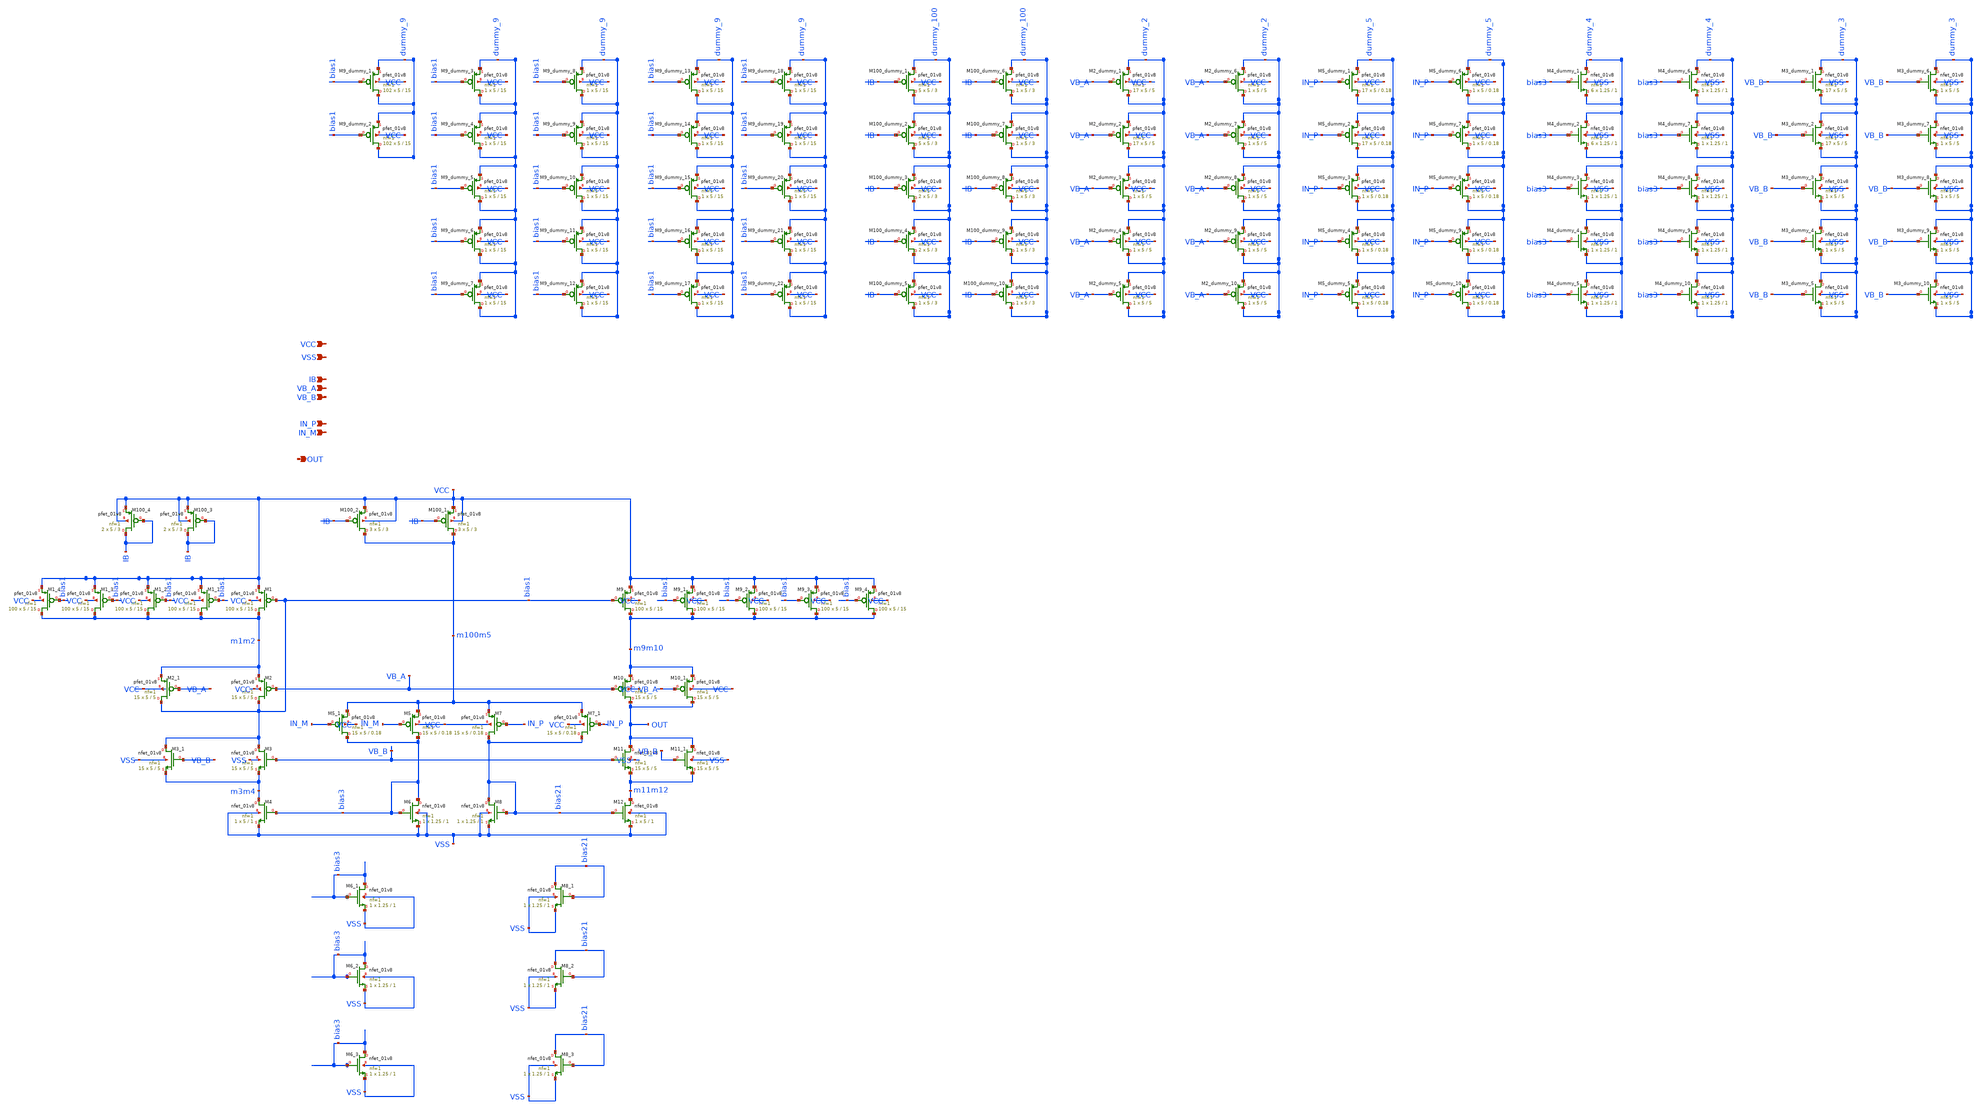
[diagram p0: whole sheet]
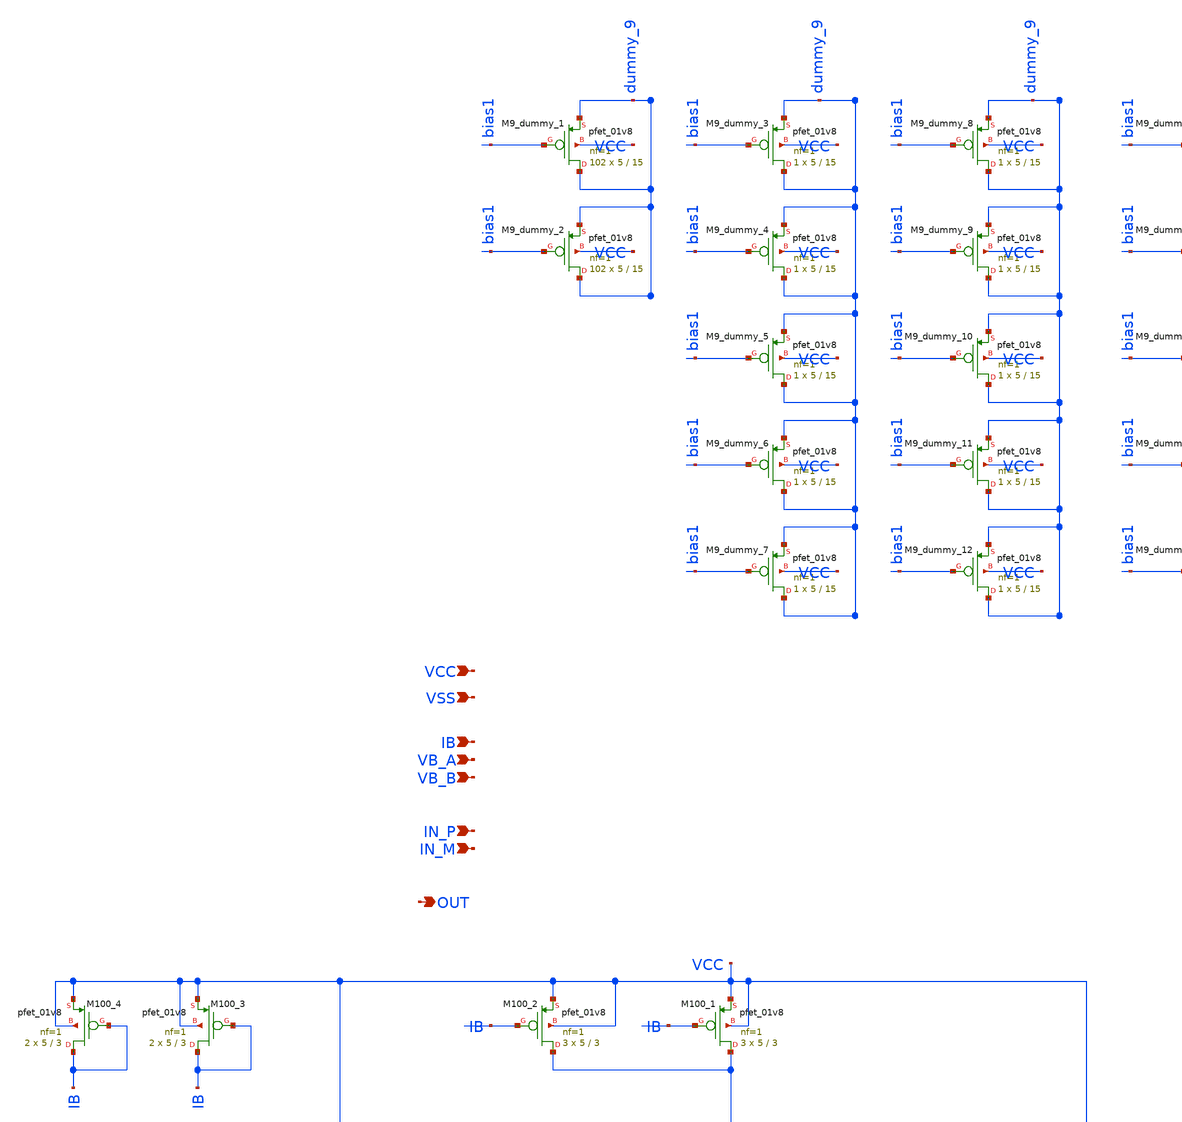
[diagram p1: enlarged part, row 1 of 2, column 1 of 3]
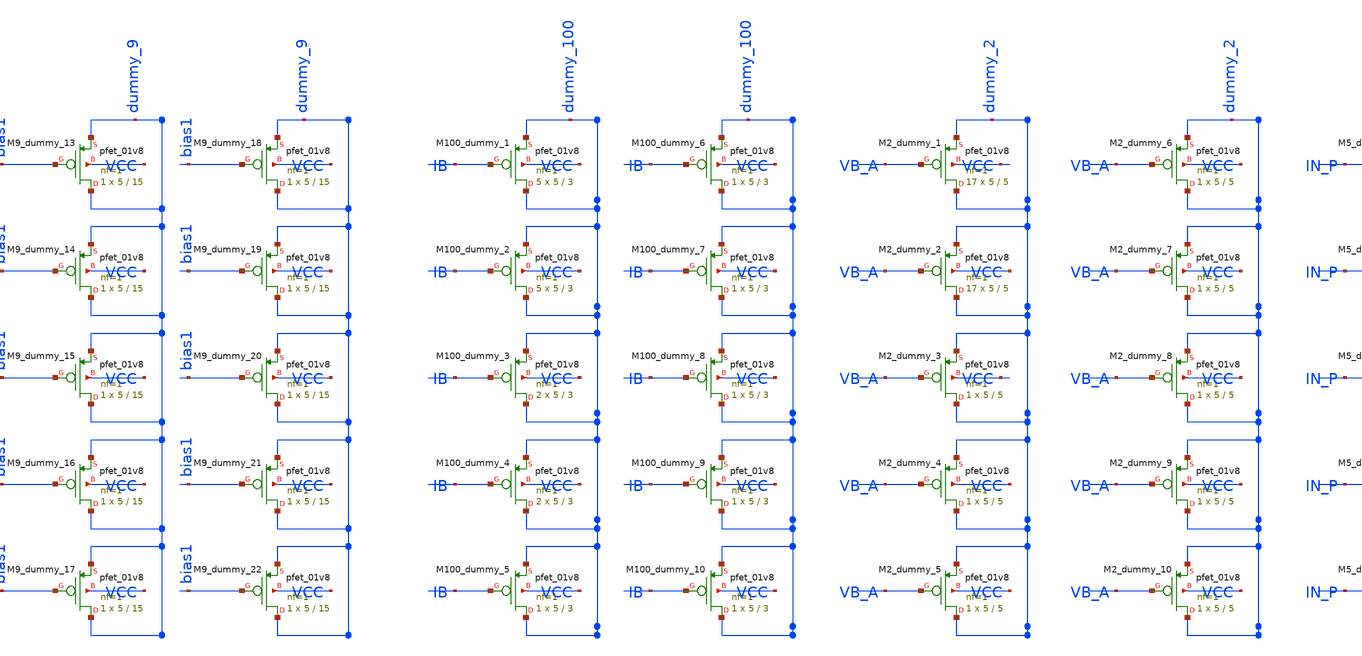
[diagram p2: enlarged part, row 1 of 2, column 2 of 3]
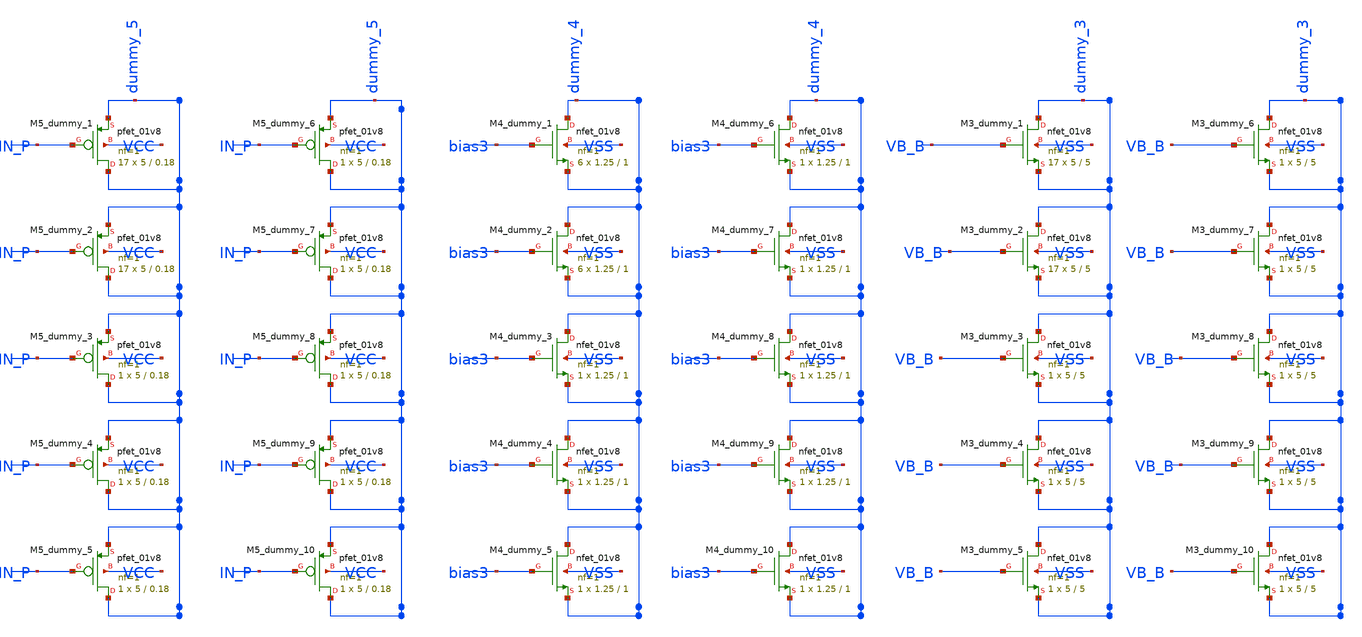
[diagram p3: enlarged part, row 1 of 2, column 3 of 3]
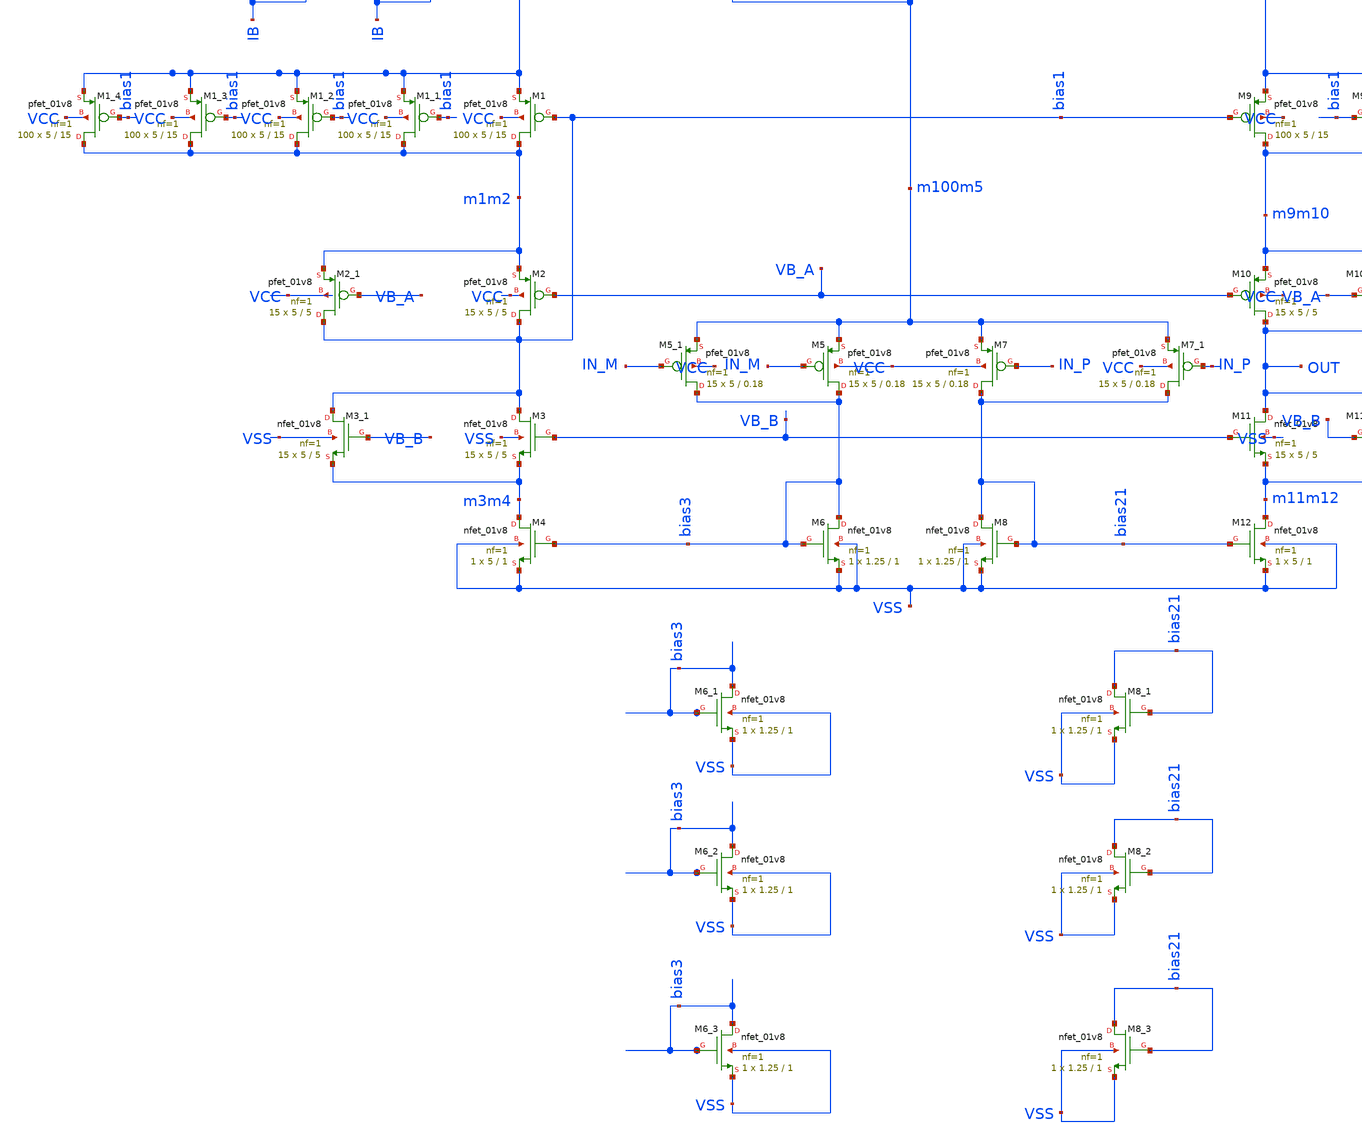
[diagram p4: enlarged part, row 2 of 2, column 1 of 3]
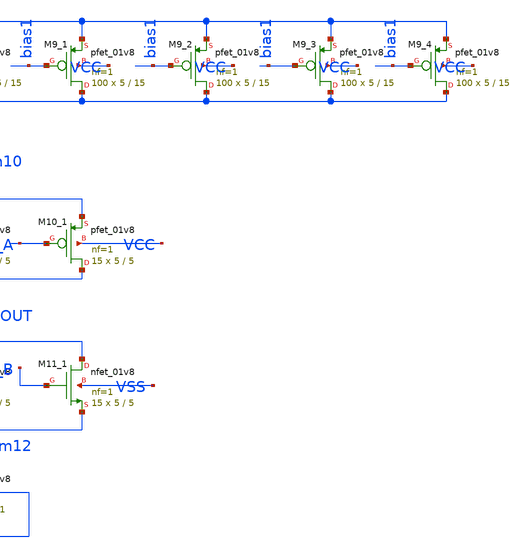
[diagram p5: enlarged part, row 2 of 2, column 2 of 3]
** sch_path: 03_Layout/opamp_cascode.sch
**.subckt opamp_cascode IN_P IN_M VCC VSS OUT VB_A VB_B IB
*.ipin IN_P
*.ipin IN_M
*.ipin VCC
*.ipin VSS
*.opin OUT
*.ipin VB_A
*.ipin VB_B
*.ipin IB
XM100_3 IB IB VCC VCC sky130_fd_pr__pfet_01v8 L=3 W=5 nf=1 ad='int((nf+1)/2) * W/nf * 0.29' as='int((nf+2)/2) * W/nf * 0.29'
+ pd='2*int((nf+1)/2) * (W/nf + 0.29)' ps='2*int((nf+2)/2) * (W/nf + 0.29)' nrd='0.29 / W' nrs='0.29 / W'
+ sa=0 sb=0 sd=0 mult=2 m=2
XM10 OUT VB_A m9m10 VCC sky130_fd_pr__pfet_01v8 L=5 W=5 nf=1 ad='int((nf+1)/2) * W/nf * 0.29' as='int((nf+2)/2) * W/nf * 0.29'
+ pd='2*int((nf+1)/2) * (W/nf + 0.29)' ps='2*int((nf+2)/2) * (W/nf + 0.29)' nrd='0.29 / W' nrs='0.29 / W'
+ sa=0 sb=0 sd=0 mult=15 m=15
XM2 bias1 VB_A m1m2 VCC sky130_fd_pr__pfet_01v8 L=5 W=5 nf=1 ad='int((nf+1)/2) * W/nf * 0.29' as='int((nf+2)/2) * W/nf * 0.29'
+ pd='2*int((nf+1)/2) * (W/nf + 0.29)' ps='2*int((nf+2)/2) * (W/nf + 0.29)' nrd='0.29 / W' nrs='0.29 / W'
+ sa=0 sb=0 sd=0 mult=15 m=15
XM5 bias3 IN_M m100m5 VCC sky130_fd_pr__pfet_01v8 L=0.18 W=5 nf=1 ad='int((nf+1)/2) * W/nf * 0.29' as='int((nf+2)/2) * W/nf * 0.29'
+ pd='2*int((nf+1)/2) * (W/nf + 0.29)' ps='2*int((nf+2)/2) * (W/nf + 0.29)' nrd='0.29 / W' nrs='0.29 / W'
+ sa=0 sb=0 sd=0 mult=15 m=15
XM7 bias21 IN_P m100m5 VCC sky130_fd_pr__pfet_01v8 L=0.18 W=5 nf=1 ad='int((nf+1)/2) * W/nf * 0.29' as='int((nf+2)/2) * W/nf * 0.29'
+ pd='2*int((nf+1)/2) * (W/nf + 0.29)' ps='2*int((nf+2)/2) * (W/nf + 0.29)' nrd='0.29 / W' nrs='0.29 / W'
+ sa=0 sb=0 sd=0 mult=15 m=15
XM6 bias3 bias3 VSS VSS sky130_fd_pr__nfet_01v8 L=1 W=1.25 nf=1 ad='int((nf+1)/2) * W/nf * 0.29' as='int((nf+2)/2) * W/nf * 0.29'
+ pd='2*int((nf+1)/2) * (W/nf + 0.29)' ps='2*int((nf+2)/2) * (W/nf + 0.29)' nrd='0.29 / W' nrs='0.29 / W'
+ sa=0 sb=0 sd=0 mult=1 m=1
XM8 bias21 bias21 VSS VSS sky130_fd_pr__nfet_01v8 L=1 W=1.25 nf=1 ad='int((nf+1)/2) * W/nf * 0.29' as='int((nf+2)/2) * W/nf * 0.29'
+ pd='2*int((nf+1)/2) * (W/nf + 0.29)' ps='2*int((nf+2)/2) * (W/nf + 0.29)' nrd='0.29 / W' nrs='0.29 / W'
+ sa=0 sb=0 sd=0 mult=1 m=1
XM12 m11m12 bias21 VSS VSS sky130_fd_pr__nfet_01v8 L=1 W=5 nf=1 ad='int((nf+1)/2) * W/nf * 0.29' as='int((nf+2)/2) * W/nf * 0.29'
+ pd='2*int((nf+1)/2) * (W/nf + 0.29)' ps='2*int((nf+2)/2) * (W/nf + 0.29)' nrd='0.29 / W' nrs='0.29 / W'
+ sa=0 sb=0 sd=0 mult=1 m=1
XM11 OUT VB_B m11m12 VSS sky130_fd_pr__nfet_01v8 L=5 W=5 nf=1 ad='int((nf+1)/2) * W/nf * 0.29' as='int((nf+2)/2) * W/nf * 0.29'
+ pd='2*int((nf+1)/2) * (W/nf + 0.29)' ps='2*int((nf+2)/2) * (W/nf + 0.29)' nrd='0.29 / W' nrs='0.29 / W'
+ sa=0 sb=0 sd=0 mult=15 m=15
XM3 bias1 VB_B m3m4 VSS sky130_fd_pr__nfet_01v8 L=5 W=5 nf=1 ad='int((nf+1)/2) * W/nf * 0.29' as='int((nf+2)/2) * W/nf * 0.29'
+ pd='2*int((nf+1)/2) * (W/nf + 0.29)' ps='2*int((nf+2)/2) * (W/nf + 0.29)' nrd='0.29 / W' nrs='0.29 / W'
+ sa=0 sb=0 sd=0 mult=15 m=15
XM100_1 m100m5 IB VCC VCC sky130_fd_pr__pfet_01v8 L=3 W=5 nf=1 ad='int((nf+1)/2) * W/nf * 0.29' as='int((nf+2)/2) * W/nf * 0.29'
+ pd='2*int((nf+1)/2) * (W/nf + 0.29)' ps='2*int((nf+2)/2) * (W/nf + 0.29)' nrd='0.29 / W' nrs='0.29 / W'
+ sa=0 sb=0 sd=0 mult=3 m=3
XM5_1 bias3 IN_M m100m5 VCC sky130_fd_pr__pfet_01v8 L=0.18 W=5 nf=1 ad='int((nf+1)/2) * W/nf * 0.29'
+ as='int((nf+2)/2) * W/nf * 0.29' pd='2*int((nf+1)/2) * (W/nf + 0.29)' ps='2*int((nf+2)/2) * (W/nf + 0.29)'
+ nrd='0.29 / W' nrs='0.29 / W' sa=0 sb=0 sd=0 mult=15 m=15
XM7_1 bias21 IN_P m100m5 VCC sky130_fd_pr__pfet_01v8 L=0.18 W=5 nf=1 ad='int((nf+1)/2) * W/nf * 0.29'
+ as='int((nf+2)/2) * W/nf * 0.29' pd='2*int((nf+1)/2) * (W/nf + 0.29)' ps='2*int((nf+2)/2) * (W/nf + 0.29)'
+ nrd='0.29 / W' nrs='0.29 / W' sa=0 sb=0 sd=0 mult=15 m=15
XM9 m9m10 bias1 VCC VCC sky130_fd_pr__pfet_01v8 L=15 W=5 nf=1 ad='int((nf+1)/2) * W/nf * 0.29' as='int((nf+2)/2) * W/nf * 0.29'
+ pd='2*int((nf+1)/2) * (W/nf + 0.29)' ps='2*int((nf+2)/2) * (W/nf + 0.29)' nrd='0.29 / W' nrs='0.29 / W'
+ sa=0 sb=0 sd=0 mult=100 m=100
XM9_1 m9m10 bias1 VCC VCC sky130_fd_pr__pfet_01v8 L=15 W=5 nf=1 ad='int((nf+1)/2) * W/nf * 0.29' as='int((nf+2)/2) * W/nf * 0.29'
+ pd='2*int((nf+1)/2) * (W/nf + 0.29)' ps='2*int((nf+2)/2) * (W/nf + 0.29)' nrd='0.29 / W' nrs='0.29 / W'
+ sa=0 sb=0 sd=0 mult=100 m=100
XM9_2 m9m10 bias1 VCC VCC sky130_fd_pr__pfet_01v8 L=15 W=5 nf=1 ad='int((nf+1)/2) * W/nf * 0.29' as='int((nf+2)/2) * W/nf * 0.29'
+ pd='2*int((nf+1)/2) * (W/nf + 0.29)' ps='2*int((nf+2)/2) * (W/nf + 0.29)' nrd='0.29 / W' nrs='0.29 / W'
+ sa=0 sb=0 sd=0 mult=100 m=100
XM9_3 m9m10 bias1 VCC VCC sky130_fd_pr__pfet_01v8 L=15 W=5 nf=1 ad='int((nf+1)/2) * W/nf * 0.29' as='int((nf+2)/2) * W/nf * 0.29'
+ pd='2*int((nf+1)/2) * (W/nf + 0.29)' ps='2*int((nf+2)/2) * (W/nf + 0.29)' nrd='0.29 / W' nrs='0.29 / W'
+ sa=0 sb=0 sd=0 mult=100 m=100
XM9_4 m9m10 bias1 VCC VCC sky130_fd_pr__pfet_01v8 L=15 W=5 nf=1 ad='int((nf+1)/2) * W/nf * 0.29' as='int((nf+2)/2) * W/nf * 0.29'
+ pd='2*int((nf+1)/2) * (W/nf + 0.29)' ps='2*int((nf+2)/2) * (W/nf + 0.29)' nrd='0.29 / W' nrs='0.29 / W'
+ sa=0 sb=0 sd=0 mult=100 m=100
XM1 m1m2 bias1 VCC VCC sky130_fd_pr__pfet_01v8 L=15 W=5 nf=1 ad='int((nf+1)/2) * W/nf * 0.29' as='int((nf+2)/2) * W/nf * 0.29'
+ pd='2*int((nf+1)/2) * (W/nf + 0.29)' ps='2*int((nf+2)/2) * (W/nf + 0.29)' nrd='0.29 / W' nrs='0.29 / W'
+ sa=0 sb=0 sd=0 mult=100 m=100
XM1_1 m1m2 bias1 VCC VCC sky130_fd_pr__pfet_01v8 L=15 W=5 nf=1 ad='int((nf+1)/2) * W/nf * 0.29' as='int((nf+2)/2) * W/nf * 0.29'
+ pd='2*int((nf+1)/2) * (W/nf + 0.29)' ps='2*int((nf+2)/2) * (W/nf + 0.29)' nrd='0.29 / W' nrs='0.29 / W'
+ sa=0 sb=0 sd=0 mult=100 m=100
XM1_2 m1m2 bias1 VCC VCC sky130_fd_pr__pfet_01v8 L=15 W=5 nf=1 ad='int((nf+1)/2) * W/nf * 0.29' as='int((nf+2)/2) * W/nf * 0.29'
+ pd='2*int((nf+1)/2) * (W/nf + 0.29)' ps='2*int((nf+2)/2) * (W/nf + 0.29)' nrd='0.29 / W' nrs='0.29 / W'
+ sa=0 sb=0 sd=0 mult=100 m=100
XM1_3 m1m2 bias1 VCC VCC sky130_fd_pr__pfet_01v8 L=15 W=5 nf=1 ad='int((nf+1)/2) * W/nf * 0.29' as='int((nf+2)/2) * W/nf * 0.29'
+ pd='2*int((nf+1)/2) * (W/nf + 0.29)' ps='2*int((nf+2)/2) * (W/nf + 0.29)' nrd='0.29 / W' nrs='0.29 / W'
+ sa=0 sb=0 sd=0 mult=100 m=100
XM1_4 m1m2 bias1 VCC VCC sky130_fd_pr__pfet_01v8 L=15 W=5 nf=1 ad='int((nf+1)/2) * W/nf * 0.29' as='int((nf+2)/2) * W/nf * 0.29'
+ pd='2*int((nf+1)/2) * (W/nf + 0.29)' ps='2*int((nf+2)/2) * (W/nf + 0.29)' nrd='0.29 / W' nrs='0.29 / W'
+ sa=0 sb=0 sd=0 mult=100 m=100
XM100_2 m100m5 IB VCC VCC sky130_fd_pr__pfet_01v8 L=3 W=5 nf=1 ad='int((nf+1)/2) * W/nf * 0.29' as='int((nf+2)/2) * W/nf * 0.29'
+ pd='2*int((nf+1)/2) * (W/nf + 0.29)' ps='2*int((nf+2)/2) * (W/nf + 0.29)' nrd='0.29 / W' nrs='0.29 / W'
+ sa=0 sb=0 sd=0 mult=3 m=3
XM10_1 OUT VB_A m9m10 VCC sky130_fd_pr__pfet_01v8 L=5 W=5 nf=1 ad='int((nf+1)/2) * W/nf * 0.29' as='int((nf+2)/2) * W/nf * 0.29'
+ pd='2*int((nf+1)/2) * (W/nf + 0.29)' ps='2*int((nf+2)/2) * (W/nf + 0.29)' nrd='0.29 / W' nrs='0.29 / W'
+ sa=0 sb=0 sd=0 mult=15 m=15
XM2_1 bias1 VB_A m1m2 VCC sky130_fd_pr__pfet_01v8 L=5 W=5 nf=1 ad='int((nf+1)/2) * W/nf * 0.29' as='int((nf+2)/2) * W/nf * 0.29'
+ pd='2*int((nf+1)/2) * (W/nf + 0.29)' ps='2*int((nf+2)/2) * (W/nf + 0.29)' nrd='0.29 / W' nrs='0.29 / W'
+ sa=0 sb=0 sd=0 mult=15 m=15
XM3_1 bias1 VB_B m3m4 VSS sky130_fd_pr__nfet_01v8 L=5 W=5 nf=1 ad='int((nf+1)/2) * W/nf * 0.29' as='int((nf+2)/2) * W/nf * 0.29'
+ pd='2*int((nf+1)/2) * (W/nf + 0.29)' ps='2*int((nf+2)/2) * (W/nf + 0.29)' nrd='0.29 / W' nrs='0.29 / W'
+ sa=0 sb=0 sd=0 mult=15 m=15
XM11_1 OUT VB_B m11m12 VSS sky130_fd_pr__nfet_01v8 L=5 W=5 nf=1 ad='int((nf+1)/2) * W/nf * 0.29' as='int((nf+2)/2) * W/nf * 0.29'
+ pd='2*int((nf+1)/2) * (W/nf + 0.29)' ps='2*int((nf+2)/2) * (W/nf + 0.29)' nrd='0.29 / W' nrs='0.29 / W'
+ sa=0 sb=0 sd=0 mult=15 m=15
XM4 m3m4 bias3 VSS VSS sky130_fd_pr__nfet_01v8 L=1 W=5 nf=1 ad='int((nf+1)/2) * W/nf * 0.29' as='int((nf+2)/2) * W/nf * 0.29'
+ pd='2*int((nf+1)/2) * (W/nf + 0.29)' ps='2*int((nf+2)/2) * (W/nf + 0.29)' nrd='0.29 / W' nrs='0.29 / W'
+ sa=0 sb=0 sd=0 mult=1 m=1
XM6_1 bias3 bias3 VSS VSS sky130_fd_pr__nfet_01v8 L=1 W=1.25 nf=1 ad='int((nf+1)/2) * W/nf * 0.29' as='int((nf+2)/2) * W/nf * 0.29'
+ pd='2*int((nf+1)/2) * (W/nf + 0.29)' ps='2*int((nf+2)/2) * (W/nf + 0.29)' nrd='0.29 / W' nrs='0.29 / W'
+ sa=0 sb=0 sd=0 mult=1 m=1
XM8_1 bias21 bias21 VSS VSS sky130_fd_pr__nfet_01v8 L=1 W=1.25 nf=1 ad='int((nf+1)/2) * W/nf * 0.29'
+ as='int((nf+2)/2) * W/nf * 0.29' pd='2*int((nf+1)/2) * (W/nf + 0.29)' ps='2*int((nf+2)/2) * (W/nf + 0.29)'
+ nrd='0.29 / W' nrs='0.29 / W' sa=0 sb=0 sd=0 mult=1 m=1
XM6_2 bias3 bias3 VSS VSS sky130_fd_pr__nfet_01v8 L=1 W=1.25 nf=1 ad='int((nf+1)/2) * W/nf * 0.29' as='int((nf+2)/2) * W/nf * 0.29'
+ pd='2*int((nf+1)/2) * (W/nf + 0.29)' ps='2*int((nf+2)/2) * (W/nf + 0.29)' nrd='0.29 / W' nrs='0.29 / W'
+ sa=0 sb=0 sd=0 mult=1 m=1
XM6_3 bias3 bias3 VSS VSS sky130_fd_pr__nfet_01v8 L=1 W=1.25 nf=1 ad='int((nf+1)/2) * W/nf * 0.29' as='int((nf+2)/2) * W/nf * 0.29'
+ pd='2*int((nf+1)/2) * (W/nf + 0.29)' ps='2*int((nf+2)/2) * (W/nf + 0.29)' nrd='0.29 / W' nrs='0.29 / W'
+ sa=0 sb=0 sd=0 mult=1 m=1
XM9_dummy_1 dummy_9 bias1 dummy_9 VCC sky130_fd_pr__pfet_01v8 L=15 W=5 nf=1 ad='int((nf+1)/2) * W/nf * 0.29'
+ as='int((nf+2)/2) * W/nf * 0.29' pd='2*int((nf+1)/2) * (W/nf + 0.29)' ps='2*int((nf+2)/2) * (W/nf + 0.29)'
+ nrd='0.29 / W' nrs='0.29 / W' sa=0 sb=0 sd=0 mult=102 m=102
XM9_dummy_2 dummy_9 bias1 dummy_9 VCC sky130_fd_pr__pfet_01v8 L=15 W=5 nf=1 ad='int((nf+1)/2) * W/nf * 0.29'
+ as='int((nf+2)/2) * W/nf * 0.29' pd='2*int((nf+1)/2) * (W/nf + 0.29)' ps='2*int((nf+2)/2) * (W/nf + 0.29)'
+ nrd='0.29 / W' nrs='0.29 / W' sa=0 sb=0 sd=0 mult=102 m=102
XM9_dummy_3 dummy_9 bias1 dummy_9 VCC sky130_fd_pr__pfet_01v8 L=15 W=5 nf=1 ad='int((nf+1)/2) * W/nf * 0.29'
+ as='int((nf+2)/2) * W/nf * 0.29' pd='2*int((nf+1)/2) * (W/nf + 0.29)' ps='2*int((nf+2)/2) * (W/nf + 0.29)'
+ nrd='0.29 / W' nrs='0.29 / W' sa=0 sb=0 sd=0 mult=1 m=1
XM9_dummy_4 dummy_9 bias1 dummy_9 VCC sky130_fd_pr__pfet_01v8 L=15 W=5 nf=1 ad='int((nf+1)/2) * W/nf * 0.29'
+ as='int((nf+2)/2) * W/nf * 0.29' pd='2*int((nf+1)/2) * (W/nf + 0.29)' ps='2*int((nf+2)/2) * (W/nf + 0.29)'
+ nrd='0.29 / W' nrs='0.29 / W' sa=0 sb=0 sd=0 mult=1 m=1
XM9_dummy_5 dummy_9 bias1 dummy_9 VCC sky130_fd_pr__pfet_01v8 L=15 W=5 nf=1 ad='int((nf+1)/2) * W/nf * 0.29'
+ as='int((nf+2)/2) * W/nf * 0.29' pd='2*int((nf+1)/2) * (W/nf + 0.29)' ps='2*int((nf+2)/2) * (W/nf + 0.29)'
+ nrd='0.29 / W' nrs='0.29 / W' sa=0 sb=0 sd=0 mult=1 m=1
XM9_dummy_6 dummy_9 bias1 dummy_9 VCC sky130_fd_pr__pfet_01v8 L=15 W=5 nf=1 ad='int((nf+1)/2) * W/nf * 0.29'
+ as='int((nf+2)/2) * W/nf * 0.29' pd='2*int((nf+1)/2) * (W/nf + 0.29)' ps='2*int((nf+2)/2) * (W/nf + 0.29)'
+ nrd='0.29 / W' nrs='0.29 / W' sa=0 sb=0 sd=0 mult=1 m=1
XM9_dummy_7 dummy_9 bias1 dummy_9 VCC sky130_fd_pr__pfet_01v8 L=15 W=5 nf=1 ad='int((nf+1)/2) * W/nf * 0.29'
+ as='int((nf+2)/2) * W/nf * 0.29' pd='2*int((nf+1)/2) * (W/nf + 0.29)' ps='2*int((nf+2)/2) * (W/nf + 0.29)'
+ nrd='0.29 / W' nrs='0.29 / W' sa=0 sb=0 sd=0 mult=1 m=1
XM9_dummy_8 dummy_9 bias1 dummy_9 VCC sky130_fd_pr__pfet_01v8 L=15 W=5 nf=1 ad='int((nf+1)/2) * W/nf * 0.29'
+ as='int((nf+2)/2) * W/nf * 0.29' pd='2*int((nf+1)/2) * (W/nf + 0.29)' ps='2*int((nf+2)/2) * (W/nf + 0.29)'
+ nrd='0.29 / W' nrs='0.29 / W' sa=0 sb=0 sd=0 mult=1 m=1
XM9_dummy_9 dummy_9 bias1 dummy_9 VCC sky130_fd_pr__pfet_01v8 L=15 W=5 nf=1 ad='int((nf+1)/2) * W/nf * 0.29'
+ as='int((nf+2)/2) * W/nf * 0.29' pd='2*int((nf+1)/2) * (W/nf + 0.29)' ps='2*int((nf+2)/2) * (W/nf + 0.29)'
+ nrd='0.29 / W' nrs='0.29 / W' sa=0 sb=0 sd=0 mult=1 m=1
XM9_dummy_10 dummy_9 bias1 dummy_9 VCC sky130_fd_pr__pfet_01v8 L=15 W=5 nf=1 ad='int((nf+1)/2) * W/nf * 0.29'
+ as='int((nf+2)/2) * W/nf * 0.29' pd='2*int((nf+1)/2) * (W/nf + 0.29)' ps='2*int((nf+2)/2) * (W/nf + 0.29)'
+ nrd='0.29 / W' nrs='0.29 / W' sa=0 sb=0 sd=0 mult=1 m=1
XM9_dummy_11 dummy_9 bias1 dummy_9 VCC sky130_fd_pr__pfet_01v8 L=15 W=5 nf=1 ad='int((nf+1)/2) * W/nf * 0.29'
+ as='int((nf+2)/2) * W/nf * 0.29' pd='2*int((nf+1)/2) * (W/nf + 0.29)' ps='2*int((nf+2)/2) * (W/nf + 0.29)'
+ nrd='0.29 / W' nrs='0.29 / W' sa=0 sb=0 sd=0 mult=1 m=1
XM9_dummy_12 dummy_9 bias1 dummy_9 VCC sky130_fd_pr__pfet_01v8 L=15 W=5 nf=1 ad='int((nf+1)/2) * W/nf * 0.29'
+ as='int((nf+2)/2) * W/nf * 0.29' pd='2*int((nf+1)/2) * (W/nf + 0.29)' ps='2*int((nf+2)/2) * (W/nf + 0.29)'
+ nrd='0.29 / W' nrs='0.29 / W' sa=0 sb=0 sd=0 mult=1 m=1
XM100_dummy_1 dummy_100 IB dummy_100 VCC sky130_fd_pr__pfet_01v8 L=3 W=5 nf=1 ad='int((nf+1)/2) * W/nf * 0.29'
+ as='int((nf+2)/2) * W/nf * 0.29' pd='2*int((nf+1)/2) * (W/nf + 0.29)' ps='2*int((nf+2)/2) * (W/nf + 0.29)'
+ nrd='0.29 / W' nrs='0.29 / W' sa=0 sb=0 sd=0 mult=5 m=5
XM100_dummy_2 dummy_100 IB dummy_100 VCC sky130_fd_pr__pfet_01v8 L=3 W=5 nf=1 ad='int((nf+1)/2) * W/nf * 0.29'
+ as='int((nf+2)/2) * W/nf * 0.29' pd='2*int((nf+1)/2) * (W/nf + 0.29)' ps='2*int((nf+2)/2) * (W/nf + 0.29)'
+ nrd='0.29 / W' nrs='0.29 / W' sa=0 sb=0 sd=0 mult=5 m=5
XM100_dummy_3 dummy_100 IB dummy_100 VCC sky130_fd_pr__pfet_01v8 L=3 W=5 nf=1 ad='int((nf+1)/2) * W/nf * 0.29'
+ as='int((nf+2)/2) * W/nf * 0.29' pd='2*int((nf+1)/2) * (W/nf + 0.29)' ps='2*int((nf+2)/2) * (W/nf + 0.29)'
+ nrd='0.29 / W' nrs='0.29 / W' sa=0 sb=0 sd=0 mult=2 m=2
XM100_dummy_4 dummy_100 IB dummy_100 VCC sky130_fd_pr__pfet_01v8 L=3 W=5 nf=1 ad='int((nf+1)/2) * W/nf * 0.29'
+ as='int((nf+2)/2) * W/nf * 0.29' pd='2*int((nf+1)/2) * (W/nf + 0.29)' ps='2*int((nf+2)/2) * (W/nf + 0.29)'
+ nrd='0.29 / W' nrs='0.29 / W' sa=0 sb=0 sd=0 mult=2 m=2
XM100_dummy_5 dummy_100 IB dummy_100 VCC sky130_fd_pr__pfet_01v8 L=3 W=5 nf=1 ad='int((nf+1)/2) * W/nf * 0.29'
+ as='int((nf+2)/2) * W/nf * 0.29' pd='2*int((nf+1)/2) * (W/nf + 0.29)' ps='2*int((nf+2)/2) * (W/nf + 0.29)'
+ nrd='0.29 / W' nrs='0.29 / W' sa=0 sb=0 sd=0 mult=1 m=1
XM100_dummy_6 dummy_100 IB dummy_100 VCC sky130_fd_pr__pfet_01v8 L=3 W=5 nf=1 ad='int((nf+1)/2) * W/nf * 0.29'
+ as='int((nf+2)/2) * W/nf * 0.29' pd='2*int((nf+1)/2) * (W/nf + 0.29)' ps='2*int((nf+2)/2) * (W/nf + 0.29)'
+ nrd='0.29 / W' nrs='0.29 / W' sa=0 sb=0 sd=0 mult=1 m=1
XM100_dummy_7 dummy_100 IB dummy_100 VCC sky130_fd_pr__pfet_01v8 L=3 W=5 nf=1 ad='int((nf+1)/2) * W/nf * 0.29'
+ as='int((nf+2)/2) * W/nf * 0.29' pd='2*int((nf+1)/2) * (W/nf + 0.29)' ps='2*int((nf+2)/2) * (W/nf + 0.29)'
+ nrd='0.29 / W' nrs='0.29 / W' sa=0 sb=0 sd=0 mult=1 m=1
XM100_dummy_8 dummy_100 IB dummy_100 VCC sky130_fd_pr__pfet_01v8 L=3 W=5 nf=1 ad='int((nf+1)/2) * W/nf * 0.29'
+ as='int((nf+2)/2) * W/nf * 0.29' pd='2*int((nf+1)/2) * (W/nf + 0.29)' ps='2*int((nf+2)/2) * (W/nf + 0.29)'
+ nrd='0.29 / W' nrs='0.29 / W' sa=0 sb=0 sd=0 mult=1 m=1
XM100_dummy_9 dummy_100 IB dummy_100 VCC sky130_fd_pr__pfet_01v8 L=3 W=5 nf=1 ad='int((nf+1)/2) * W/nf * 0.29'
+ as='int((nf+2)/2) * W/nf * 0.29' pd='2*int((nf+1)/2) * (W/nf + 0.29)' ps='2*int((nf+2)/2) * (W/nf + 0.29)'
+ nrd='0.29 / W' nrs='0.29 / W' sa=0 sb=0 sd=0 mult=1 m=1
XM100_dummy_10 dummy_100 IB dummy_100 VCC sky130_fd_pr__pfet_01v8 L=3 W=5 nf=1 ad='int((nf+1)/2) * W/nf * 0.29'
+ as='int((nf+2)/2) * W/nf * 0.29' pd='2*int((nf+1)/2) * (W/nf + 0.29)' ps='2*int((nf+2)/2) * (W/nf + 0.29)'
+ nrd='0.29 / W' nrs='0.29 / W' sa=0 sb=0 sd=0 mult=1 m=1
XM2_dummy_1 dummy_2 VB_A dummy_2 VCC sky130_fd_pr__pfet_01v8 L=5 W=5 nf=1 ad='int((nf+1)/2) * W/nf * 0.29'
+ as='int((nf+2)/2) * W/nf * 0.29' pd='2*int((nf+1)/2) * (W/nf + 0.29)' ps='2*int((nf+2)/2) * (W/nf + 0.29)'
+ nrd='0.29 / W' nrs='0.29 / W' sa=0 sb=0 sd=0 mult=17 m=17
XM2_dummy_2 dummy_2 VB_A dummy_2 VCC sky130_fd_pr__pfet_01v8 L=5 W=5 nf=1 ad='int((nf+1)/2) * W/nf * 0.29'
+ as='int((nf+2)/2) * W/nf * 0.29' pd='2*int((nf+1)/2) * (W/nf + 0.29)' ps='2*int((nf+2)/2) * (W/nf + 0.29)'
+ nrd='0.29 / W' nrs='0.29 / W' sa=0 sb=0 sd=0 mult=17 m=17
XM2_dummy_3 dummy_2 VB_A dummy_2 VCC sky130_fd_pr__pfet_01v8 L=5 W=5 nf=1 ad='int((nf+1)/2) * W/nf * 0.29'
+ as='int((nf+2)/2) * W/nf * 0.29' pd='2*int((nf+1)/2) * (W/nf + 0.29)' ps='2*int((nf+2)/2) * (W/nf + 0.29)'
+ nrd='0.29 / W' nrs='0.29 / W' sa=0 sb=0 sd=0 mult=1 m=1
XM2_dummy_4 dummy_2 VB_A dummy_2 VCC sky130_fd_pr__pfet_01v8 L=5 W=5 nf=1 ad='int((nf+1)/2) * W/nf * 0.29'
+ as='int((nf+2)/2) * W/nf * 0.29' pd='2*int((nf+1)/2) * (W/nf + 0.29)' ps='2*int((nf+2)/2) * (W/nf + 0.29)'
+ nrd='0.29 / W' nrs='0.29 / W' sa=0 sb=0 sd=0 mult=1 m=1
XM2_dummy_5 dummy_2 VB_A dummy_2 VCC sky130_fd_pr__pfet_01v8 L=5 W=5 nf=1 ad='int((nf+1)/2) * W/nf * 0.29'
+ as='int((nf+2)/2) * W/nf * 0.29' pd='2*int((nf+1)/2) * (W/nf + 0.29)' ps='2*int((nf+2)/2) * (W/nf + 0.29)'
+ nrd='0.29 / W' nrs='0.29 / W' sa=0 sb=0 sd=0 mult=1 m=1
XM2_dummy_6 dummy_2 VB_A dummy_2 VCC sky130_fd_pr__pfet_01v8 L=5 W=5 nf=1 ad='int((nf+1)/2) * W/nf * 0.29'
+ as='int((nf+2)/2) * W/nf * 0.29' pd='2*int((nf+1)/2) * (W/nf + 0.29)' ps='2*int((nf+2)/2) * (W/nf + 0.29)'
+ nrd='0.29 / W' nrs='0.29 / W' sa=0 sb=0 sd=0 mult=1 m=1
XM2_dummy_7 dummy_2 VB_A dummy_2 VCC sky130_fd_pr__pfet_01v8 L=5 W=5 nf=1 ad='int((nf+1)/2) * W/nf * 0.29'
+ as='int((nf+2)/2) * W/nf * 0.29' pd='2*int((nf+1)/2) * (W/nf + 0.29)' ps='2*int((nf+2)/2) * (W/nf + 0.29)'
+ nrd='0.29 / W' nrs='0.29 / W' sa=0 sb=0 sd=0 mult=1 m=1
XM2_dummy_8 dummy_2 VB_A dummy_2 VCC sky130_fd_pr__pfet_01v8 L=5 W=5 nf=1 ad='int((nf+1)/2) * W/nf * 0.29'
+ as='int((nf+2)/2) * W/nf * 0.29' pd='2*int((nf+1)/2) * (W/nf + 0.29)' ps='2*int((nf+2)/2) * (W/nf + 0.29)'
+ nrd='0.29 / W' nrs='0.29 / W' sa=0 sb=0 sd=0 mult=1 m=1
XM2_dummy_9 dummy_2 VB_A dummy_2 VCC sky130_fd_pr__pfet_01v8 L=5 W=5 nf=1 ad='int((nf+1)/2) * W/nf * 0.29'
+ as='int((nf+2)/2) * W/nf * 0.29' pd='2*int((nf+1)/2) * (W/nf + 0.29)' ps='2*int((nf+2)/2) * (W/nf + 0.29)'
+ nrd='0.29 / W' nrs='0.29 / W' sa=0 sb=0 sd=0 mult=1 m=1
XM2_dummy_10 dummy_2 VB_A dummy_2 VCC sky130_fd_pr__pfet_01v8 L=5 W=5 nf=1 ad='int((nf+1)/2) * W/nf * 0.29'
+ as='int((nf+2)/2) * W/nf * 0.29' pd='2*int((nf+1)/2) * (W/nf + 0.29)' ps='2*int((nf+2)/2) * (W/nf + 0.29)'
+ nrd='0.29 / W' nrs='0.29 / W' sa=0 sb=0 sd=0 mult=1 m=1
XM5_dummy_1 dummy_5 IN_P dummy_5 VCC sky130_fd_pr__pfet_01v8 L=0.18 W=5 nf=1 ad='int((nf+1)/2) * W/nf * 0.29'
+ as='int((nf+2)/2) * W/nf * 0.29' pd='2*int((nf+1)/2) * (W/nf + 0.29)' ps='2*int((nf+2)/2) * (W/nf + 0.29)'
+ nrd='0.29 / W' nrs='0.29 / W' sa=0 sb=0 sd=0 mult=17 m=17
XM5_dummy_2 dummy_5 IN_P dummy_5 VCC sky130_fd_pr__pfet_01v8 L=0.18 W=5 nf=1 ad='int((nf+1)/2) * W/nf * 0.29'
+ as='int((nf+2)/2) * W/nf * 0.29' pd='2*int((nf+1)/2) * (W/nf + 0.29)' ps='2*int((nf+2)/2) * (W/nf + 0.29)'
+ nrd='0.29 / W' nrs='0.29 / W' sa=0 sb=0 sd=0 mult=17 m=17
XM5_dummy_3 dummy_5 IN_P dummy_5 VCC sky130_fd_pr__pfet_01v8 L=0.18 W=5 nf=1 ad='int((nf+1)/2) * W/nf * 0.29'
+ as='int((nf+2)/2) * W/nf * 0.29' pd='2*int((nf+1)/2) * (W/nf + 0.29)' ps='2*int((nf+2)/2) * (W/nf + 0.29)'
+ nrd='0.29 / W' nrs='0.29 / W' sa=0 sb=0 sd=0 mult=1 m=1
XM5_dummy_4 dummy_5 IN_P dummy_5 VCC sky130_fd_pr__pfet_01v8 L=0.18 W=5 nf=1 ad='int((nf+1)/2) * W/nf * 0.29'
+ as='int((nf+2)/2) * W/nf * 0.29' pd='2*int((nf+1)/2) * (W/nf + 0.29)' ps='2*int((nf+2)/2) * (W/nf + 0.29)'
+ nrd='0.29 / W' nrs='0.29 / W' sa=0 sb=0 sd=0 mult=1 m=1
XM5_dummy_5 dummy_5 IN_P dummy_5 VCC sky130_fd_pr__pfet_01v8 L=0.18 W=5 nf=1 ad='int((nf+1)/2) * W/nf * 0.29'
+ as='int((nf+2)/2) * W/nf * 0.29' pd='2*int((nf+1)/2) * (W/nf + 0.29)' ps='2*int((nf+2)/2) * (W/nf + 0.29)'
+ nrd='0.29 / W' nrs='0.29 / W' sa=0 sb=0 sd=0 mult=1 m=1
XM5_dummy_6 dummy_5 IN_P dummy_5 VCC sky130_fd_pr__pfet_01v8 L=0.18 W=5 nf=1 ad='int((nf+1)/2) * W/nf * 0.29'
+ as='int((nf+2)/2) * W/nf * 0.29' pd='2*int((nf+1)/2) * (W/nf + 0.29)' ps='2*int((nf+2)/2) * (W/nf + 0.29)'
+ nrd='0.29 / W' nrs='0.29 / W' sa=0 sb=0 sd=0 mult=1 m=1
XM5_dummy_7 dummy_5 IN_P dummy_5 VCC sky130_fd_pr__pfet_01v8 L=0.18 W=5 nf=1 ad='int((nf+1)/2) * W/nf * 0.29'
+ as='int((nf+2)/2) * W/nf * 0.29' pd='2*int((nf+1)/2) * (W/nf + 0.29)' ps='2*int((nf+2)/2) * (W/nf + 0.29)'
+ nrd='0.29 / W' nrs='0.29 / W' sa=0 sb=0 sd=0 mult=1 m=1
XM5_dummy_8 dummy_5 IN_P dummy_5 VCC sky130_fd_pr__pfet_01v8 L=0.18 W=5 nf=1 ad='int((nf+1)/2) * W/nf * 0.29'
+ as='int((nf+2)/2) * W/nf * 0.29' pd='2*int((nf+1)/2) * (W/nf + 0.29)' ps='2*int((nf+2)/2) * (W/nf + 0.29)'
+ nrd='0.29 / W' nrs='0.29 / W' sa=0 sb=0 sd=0 mult=1 m=1
XM5_dummy_9 dummy_5 IN_P dummy_5 VCC sky130_fd_pr__pfet_01v8 L=0.18 W=5 nf=1 ad='int((nf+1)/2) * W/nf * 0.29'
+ as='int((nf+2)/2) * W/nf * 0.29' pd='2*int((nf+1)/2) * (W/nf + 0.29)' ps='2*int((nf+2)/2) * (W/nf + 0.29)'
+ nrd='0.29 / W' nrs='0.29 / W' sa=0 sb=0 sd=0 mult=1 m=1
XM5_dummy_10 dummy_5 IN_P dummy_5 VCC sky130_fd_pr__pfet_01v8 L=0.18 W=5 nf=1 ad='int((nf+1)/2) * W/nf * 0.29'
+ as='int((nf+2)/2) * W/nf * 0.29' pd='2*int((nf+1)/2) * (W/nf + 0.29)' ps='2*int((nf+2)/2) * (W/nf + 0.29)'
+ nrd='0.29 / W' nrs='0.29 / W' sa=0 sb=0 sd=0 mult=1 m=1
XM4_dummy_1 dummy_4 bias3 dummy_4 VSS sky130_fd_pr__nfet_01v8 L=1 W=1.25 nf=1 ad='int((nf+1)/2) * W/nf * 0.29'
+ as='int((nf+2)/2) * W/nf * 0.29' pd='2*int((nf+1)/2) * (W/nf + 0.29)' ps='2*int((nf+2)/2) * (W/nf + 0.29)'
+ nrd='0.29 / W' nrs='0.29 / W' sa=0 sb=0 sd=0 mult=6 m=6
XM4_dummy_2 dummy_4 bias3 dummy_4 VSS sky130_fd_pr__nfet_01v8 L=1 W=1.25 nf=1 ad='int((nf+1)/2) * W/nf * 0.29'
+ as='int((nf+2)/2) * W/nf * 0.29' pd='2*int((nf+1)/2) * (W/nf + 0.29)' ps='2*int((nf+2)/2) * (W/nf + 0.29)'
+ nrd='0.29 / W' nrs='0.29 / W' sa=0 sb=0 sd=0 mult=6 m=6
XM4_dummy_3 dummy_4 bias3 dummy_4 VSS sky130_fd_pr__nfet_01v8 L=1 W=1.25 nf=1 ad='int((nf+1)/2) * W/nf * 0.29'
+ as='int((nf+2)/2) * W/nf * 0.29' pd='2*int((nf+1)/2) * (W/nf + 0.29)' ps='2*int((nf+2)/2) * (W/nf + 0.29)'
+ nrd='0.29 / W' nrs='0.29 / W' sa=0 sb=0 sd=0 mult=1 m=1
XM4_dummy_4 dummy_4 bias3 dummy_4 VSS sky130_fd_pr__nfet_01v8 L=1 W=1.25 nf=1 ad='int((nf+1)/2) * W/nf * 0.29'
+ as='int((nf+2)/2) * W/nf * 0.29' pd='2*int((nf+1)/2) * (W/nf + 0.29)' ps='2*int((nf+2)/2) * (W/nf + 0.29)'
+ nrd='0.29 / W' nrs='0.29 / W' sa=0 sb=0 sd=0 mult=1 m=1
XM4_dummy_5 dummy_4 bias3 dummy_4 VSS sky130_fd_pr__nfet_01v8 L=1 W=1.25 nf=1 ad='int((nf+1)/2) * W/nf * 0.29'
+ as='int((nf+2)/2) * W/nf * 0.29' pd='2*int((nf+1)/2) * (W/nf + 0.29)' ps='2*int((nf+2)/2) * (W/nf + 0.29)'
+ nrd='0.29 / W' nrs='0.29 / W' sa=0 sb=0 sd=0 mult=1 m=1
XM4_dummy_6 dummy_4 bias3 dummy_4 VSS sky130_fd_pr__nfet_01v8 L=1 W=1.25 nf=1 ad='int((nf+1)/2) * W/nf * 0.29'
+ as='int((nf+2)/2) * W/nf * 0.29' pd='2*int((nf+1)/2) * (W/nf + 0.29)' ps='2*int((nf+2)/2) * (W/nf + 0.29)'
+ nrd='0.29 / W' nrs='0.29 / W' sa=0 sb=0 sd=0 mult=1 m=1
XM4_dummy_7 dummy_4 bias3 dummy_4 VSS sky130_fd_pr__nfet_01v8 L=1 W=1.25 nf=1 ad='int((nf+1)/2) * W/nf * 0.29'
+ as='int((nf+2)/2) * W/nf * 0.29' pd='2*int((nf+1)/2) * (W/nf + 0.29)' ps='2*int((nf+2)/2) * (W/nf + 0.29)'
+ nrd='0.29 / W' nrs='0.29 / W' sa=0 sb=0 sd=0 mult=1 m=1
XM4_dummy_8 dummy_4 bias3 dummy_4 VSS sky130_fd_pr__nfet_01v8 L=1 W=1.25 nf=1 ad='int((nf+1)/2) * W/nf * 0.29'
+ as='int((nf+2)/2) * W/nf * 0.29' pd='2*int((nf+1)/2) * (W/nf + 0.29)' ps='2*int((nf+2)/2) * (W/nf + 0.29)'
+ nrd='0.29 / W' nrs='0.29 / W' sa=0 sb=0 sd=0 mult=1 m=1
XM4_dummy_9 dummy_4 bias3 dummy_4 VSS sky130_fd_pr__nfet_01v8 L=1 W=1.25 nf=1 ad='int((nf+1)/2) * W/nf * 0.29'
+ as='int((nf+2)/2) * W/nf * 0.29' pd='2*int((nf+1)/2) * (W/nf + 0.29)' ps='2*int((nf+2)/2) * (W/nf + 0.29)'
+ nrd='0.29 / W' nrs='0.29 / W' sa=0 sb=0 sd=0 mult=1 m=1
XM4_dummy_10 dummy_4 bias3 dummy_4 VSS sky130_fd_pr__nfet_01v8 L=1 W=1.25 nf=1 ad='int((nf+1)/2) * W/nf * 0.29'
+ as='int((nf+2)/2) * W/nf * 0.29' pd='2*int((nf+1)/2) * (W/nf + 0.29)' ps='2*int((nf+2)/2) * (W/nf + 0.29)'
+ nrd='0.29 / W' nrs='0.29 / W' sa=0 sb=0 sd=0 mult=1 m=1
XM8_2 bias21 bias21 VSS VSS sky130_fd_pr__nfet_01v8 L=1 W=1.25 nf=1 ad='int((nf+1)/2) * W/nf * 0.29'
+ as='int((nf+2)/2) * W/nf * 0.29' pd='2*int((nf+1)/2) * (W/nf + 0.29)' ps='2*int((nf+2)/2) * (W/nf + 0.29)'
+ nrd='0.29 / W' nrs='0.29 / W' sa=0 sb=0 sd=0 mult=1 m=1
XM8_3 bias21 bias21 VSS VSS sky130_fd_pr__nfet_01v8 L=1 W=1.25 nf=1 ad='int((nf+1)/2) * W/nf * 0.29'
+ as='int((nf+2)/2) * W/nf * 0.29' pd='2*int((nf+1)/2) * (W/nf + 0.29)' ps='2*int((nf+2)/2) * (W/nf + 0.29)'
+ nrd='0.29 / W' nrs='0.29 / W' sa=0 sb=0 sd=0 mult=1 m=1
XM100_4 IB IB VCC VCC sky130_fd_pr__pfet_01v8 L=3 W=5 nf=1 ad='int((nf+1)/2) * W/nf * 0.29' as='int((nf+2)/2) * W/nf * 0.29'
+ pd='2*int((nf+1)/2) * (W/nf + 0.29)' ps='2*int((nf+2)/2) * (W/nf + 0.29)' nrd='0.29 / W' nrs='0.29 / W'
+ sa=0 sb=0 sd=0 mult=2 m=2
XM3_dummy_1 dummy_3 VB_B dummy_3 VSS sky130_fd_pr__nfet_01v8 L=5 W=5 nf=1 ad='int((nf+1)/2) * W/nf * 0.29'
+ as='int((nf+2)/2) * W/nf * 0.29' pd='2*int((nf+1)/2) * (W/nf + 0.29)' ps='2*int((nf+2)/2) * (W/nf + 0.29)'
+ nrd='0.29 / W' nrs='0.29 / W' sa=0 sb=0 sd=0 mult=17 m=17
XM3_dummy_2 dummy_3 VB_B dummy_3 VSS sky130_fd_pr__nfet_01v8 L=5 W=5 nf=1 ad='int((nf+1)/2) * W/nf * 0.29'
+ as='int((nf+2)/2) * W/nf * 0.29' pd='2*int((nf+1)/2) * (W/nf + 0.29)' ps='2*int((nf+2)/2) * (W/nf + 0.29)'
+ nrd='0.29 / W' nrs='0.29 / W' sa=0 sb=0 sd=0 mult=17 m=17
XM3_dummy_3 dummy_3 VB_B dummy_3 VSS sky130_fd_pr__nfet_01v8 L=5 W=5 nf=1 ad='int((nf+1)/2) * W/nf * 0.29'
+ as='int((nf+2)/2) * W/nf * 0.29' pd='2*int((nf+1)/2) * (W/nf + 0.29)' ps='2*int((nf+2)/2) * (W/nf + 0.29)'
+ nrd='0.29 / W' nrs='0.29 / W' sa=0 sb=0 sd=0 mult=1 m=1
XM3_dummy_4 dummy_3 VB_B dummy_3 VSS sky130_fd_pr__nfet_01v8 L=5 W=5 nf=1 ad='int((nf+1)/2) * W/nf * 0.29'
+ as='int((nf+2)/2) * W/nf * 0.29' pd='2*int((nf+1)/2) * (W/nf + 0.29)' ps='2*int((nf+2)/2) * (W/nf + 0.29)'
+ nrd='0.29 / W' nrs='0.29 / W' sa=0 sb=0 sd=0 mult=1 m=1
XM3_dummy_5 dummy_3 VB_B dummy_3 VSS sky130_fd_pr__nfet_01v8 L=5 W=5 nf=1 ad='int((nf+1)/2) * W/nf * 0.29'
+ as='int((nf+2)/2) * W/nf * 0.29' pd='2*int((nf+1)/2) * (W/nf + 0.29)' ps='2*int((nf+2)/2) * (W/nf + 0.29)'
+ nrd='0.29 / W' nrs='0.29 / W' sa=0 sb=0 sd=0 mult=1 m=1
XM3_dummy_6 dummy_3 VB_B dummy_3 VSS sky130_fd_pr__nfet_01v8 L=5 W=5 nf=1 ad='int((nf+1)/2) * W/nf * 0.29'
+ as='int((nf+2)/2) * W/nf * 0.29' pd='2*int((nf+1)/2) * (W/nf + 0.29)' ps='2*int((nf+2)/2) * (W/nf + 0.29)'
+ nrd='0.29 / W' nrs='0.29 / W' sa=0 sb=0 sd=0 mult=1 m=1
XM3_dummy_7 dummy_3 VB_B dummy_3 VSS sky130_fd_pr__nfet_01v8 L=5 W=5 nf=1 ad='int((nf+1)/2) * W/nf * 0.29'
+ as='int((nf+2)/2) * W/nf * 0.29' pd='2*int((nf+1)/2) * (W/nf + 0.29)' ps='2*int((nf+2)/2) * (W/nf + 0.29)'
+ nrd='0.29 / W' nrs='0.29 / W' sa=0 sb=0 sd=0 mult=1 m=1
XM3_dummy_8 dummy_3 VB_B dummy_3 VSS sky130_fd_pr__nfet_01v8 L=5 W=5 nf=1 ad='int((nf+1)/2) * W/nf * 0.29'
+ as='int((nf+2)/2) * W/nf * 0.29' pd='2*int((nf+1)/2) * (W/nf + 0.29)' ps='2*int((nf+2)/2) * (W/nf + 0.29)'
+ nrd='0.29 / W' nrs='0.29 / W' sa=0 sb=0 sd=0 mult=1 m=1
XM3_dummy_9 dummy_3 VB_B dummy_3 VSS sky130_fd_pr__nfet_01v8 L=5 W=5 nf=1 ad='int((nf+1)/2) * W/nf * 0.29'
+ as='int((nf+2)/2) * W/nf * 0.29' pd='2*int((nf+1)/2) * (W/nf + 0.29)' ps='2*int((nf+2)/2) * (W/nf + 0.29)'
+ nrd='0.29 / W' nrs='0.29 / W' sa=0 sb=0 sd=0 mult=1 m=1
XM3_dummy_10 dummy_3 VB_B dummy_3 VSS sky130_fd_pr__nfet_01v8 L=5 W=5 nf=1 ad='int((nf+1)/2) * W/nf * 0.29'
+ as='int((nf+2)/2) * W/nf * 0.29' pd='2*int((nf+1)/2) * (W/nf + 0.29)' ps='2*int((nf+2)/2) * (W/nf + 0.29)'
+ nrd='0.29 / W' nrs='0.29 / W' sa=0 sb=0 sd=0 mult=1 m=1
XM9_dummy_13 dummy_9 bias1 dummy_9 VCC sky130_fd_pr__pfet_01v8 L=15 W=5 nf=1 ad='int((nf+1)/2) * W/nf * 0.29'
+ as='int((nf+2)/2) * W/nf * 0.29' pd='2*int((nf+1)/2) * (W/nf + 0.29)' ps='2*int((nf+2)/2) * (W/nf + 0.29)'
+ nrd='0.29 / W' nrs='0.29 / W' sa=0 sb=0 sd=0 mult=1 m=1
XM9_dummy_14 dummy_9 bias1 dummy_9 VCC sky130_fd_pr__pfet_01v8 L=15 W=5 nf=1 ad='int((nf+1)/2) * W/nf * 0.29'
+ as='int((nf+2)/2) * W/nf * 0.29' pd='2*int((nf+1)/2) * (W/nf + 0.29)' ps='2*int((nf+2)/2) * (W/nf + 0.29)'
+ nrd='0.29 / W' nrs='0.29 / W' sa=0 sb=0 sd=0 mult=1 m=1
XM9_dummy_15 dummy_9 bias1 dummy_9 VCC sky130_fd_pr__pfet_01v8 L=15 W=5 nf=1 ad='int((nf+1)/2) * W/nf * 0.29'
+ as='int((nf+2)/2) * W/nf * 0.29' pd='2*int((nf+1)/2) * (W/nf + 0.29)' ps='2*int((nf+2)/2) * (W/nf + 0.29)'
+ nrd='0.29 / W' nrs='0.29 / W' sa=0 sb=0 sd=0 mult=1 m=1
XM9_dummy_16 dummy_9 bias1 dummy_9 VCC sky130_fd_pr__pfet_01v8 L=15 W=5 nf=1 ad='int((nf+1)/2) * W/nf * 0.29'
+ as='int((nf+2)/2) * W/nf * 0.29' pd='2*int((nf+1)/2) * (W/nf + 0.29)' ps='2*int((nf+2)/2) * (W/nf + 0.29)'
+ nrd='0.29 / W' nrs='0.29 / W' sa=0 sb=0 sd=0 mult=1 m=1
XM9_dummy_17 dummy_9 bias1 dummy_9 VCC sky130_fd_pr__pfet_01v8 L=15 W=5 nf=1 ad='int((nf+1)/2) * W/nf * 0.29'
+ as='int((nf+2)/2) * W/nf * 0.29' pd='2*int((nf+1)/2) * (W/nf + 0.29)' ps='2*int((nf+2)/2) * (W/nf + 0.29)'
+ nrd='0.29 / W' nrs='0.29 / W' sa=0 sb=0 sd=0 mult=1 m=1
XM9_dummy_18 dummy_9 bias1 dummy_9 VCC sky130_fd_pr__pfet_01v8 L=15 W=5 nf=1 ad='int((nf+1)/2) * W/nf * 0.29'
+ as='int((nf+2)/2) * W/nf * 0.29' pd='2*int((nf+1)/2) * (W/nf + 0.29)' ps='2*int((nf+2)/2) * (W/nf + 0.29)'
+ nrd='0.29 / W' nrs='0.29 / W' sa=0 sb=0 sd=0 mult=1 m=1
XM9_dummy_19 dummy_9 bias1 dummy_9 VCC sky130_fd_pr__pfet_01v8 L=15 W=5 nf=1 ad='int((nf+1)/2) * W/nf * 0.29'
+ as='int((nf+2)/2) * W/nf * 0.29' pd='2*int((nf+1)/2) * (W/nf + 0.29)' ps='2*int((nf+2)/2) * (W/nf + 0.29)'
+ nrd='0.29 / W' nrs='0.29 / W' sa=0 sb=0 sd=0 mult=1 m=1
XM9_dummy_20 dummy_9 bias1 dummy_9 VCC sky130_fd_pr__pfet_01v8 L=15 W=5 nf=1 ad='int((nf+1)/2) * W/nf * 0.29'
+ as='int((nf+2)/2) * W/nf * 0.29' pd='2*int((nf+1)/2) * (W/nf + 0.29)' ps='2*int((nf+2)/2) * (W/nf + 0.29)'
+ nrd='0.29 / W' nrs='0.29 / W' sa=0 sb=0 sd=0 mult=1 m=1
XM9_dummy_21 dummy_9 bias1 dummy_9 VCC sky130_fd_pr__pfet_01v8 L=15 W=5 nf=1 ad='int((nf+1)/2) * W/nf * 0.29'
+ as='int((nf+2)/2) * W/nf * 0.29' pd='2*int((nf+1)/2) * (W/nf + 0.29)' ps='2*int((nf+2)/2) * (W/nf + 0.29)'
+ nrd='0.29 / W' nrs='0.29 / W' sa=0 sb=0 sd=0 mult=1 m=1
XM9_dummy_22 dummy_9 bias1 dummy_9 VCC sky130_fd_pr__pfet_01v8 L=15 W=5 nf=1 ad='int((nf+1)/2) * W/nf * 0.29'
+ as='int((nf+2)/2) * W/nf * 0.29' pd='2*int((nf+1)/2) * (W/nf + 0.29)' ps='2*int((nf+2)/2) * (W/nf + 0.29)'
+ nrd='0.29 / W' nrs='0.29 / W' sa=0 sb=0 sd=0 mult=1 m=1
**.ends
.end
